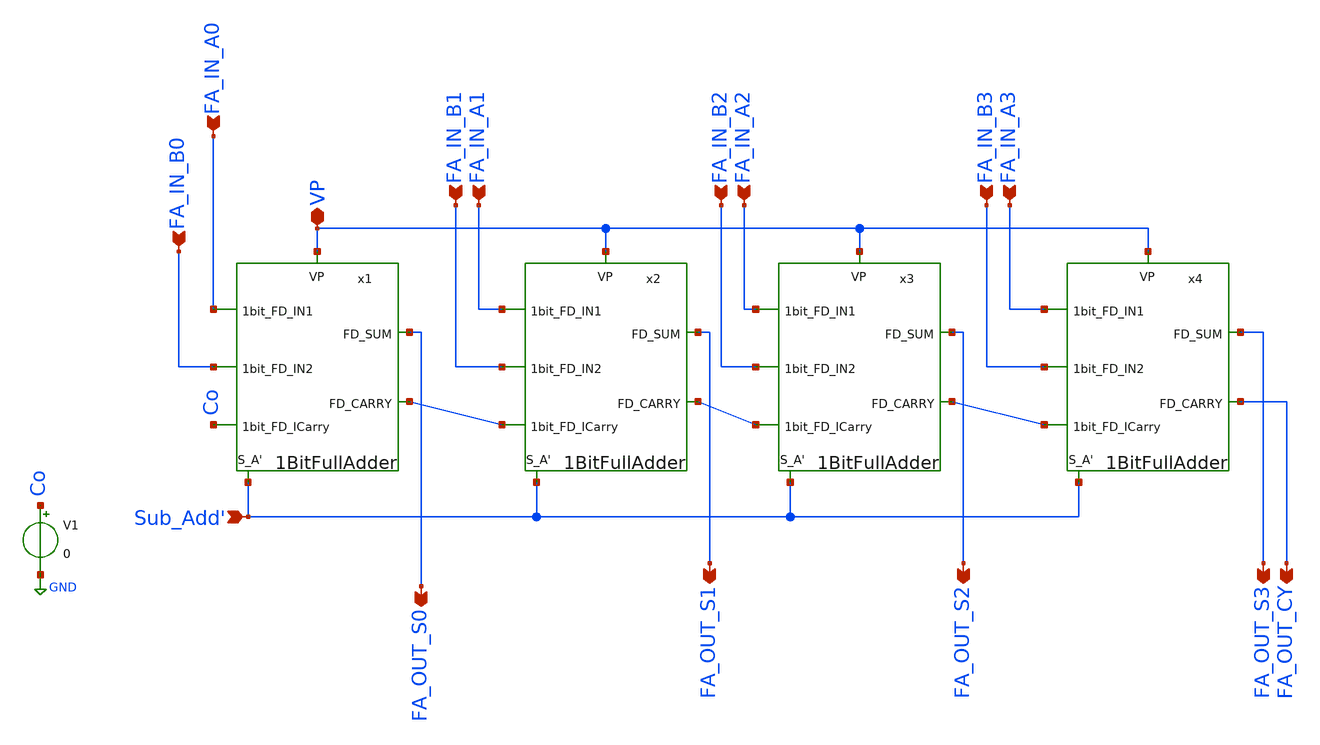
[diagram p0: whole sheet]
** sch_path: AllSymbols&Sch/AdderSubtractor/4bitFullAddSUB.sch
**.subckt 4bitFullAddSUB FA_IN_A0 VP FA_IN_B0 FA_IN_B2 FA_IN_B3 FA_IN_A2 FA_IN_A3 FA_IN_B1 FA_IN_A1 FA_OUT_S0
*+ FA_OUT_S1 FA_OUT_S2 FA_OUT_S3 FA_OUT_CY Sub_Add'
*.ipin FA_IN_A0
*.iopin VP
*.ipin FA_IN_B0
*.ipin FA_IN_B2
*.ipin FA_IN_B3
*.ipin FA_IN_A2
*.ipin FA_IN_A3
*.ipin FA_IN_B1
*.ipin FA_IN_A1
*.opin FA_OUT_S0
*.opin FA_OUT_S1
*.opin FA_OUT_S2
*.opin FA_OUT_S3
*.opin FA_OUT_CY
*.ipin Sub_Add'
V1 Co GND 0
x1 VP FA_IN_A0 FA_IN_B0 Co FA_OUT_S0 net1 Sub_Add' 1BitFullAdder
x2 VP FA_IN_A1 FA_IN_B1 net1 FA_OUT_S1 net2 Sub_Add' 1BitFullAdder
x3 VP FA_IN_A2 FA_IN_B2 net2 FA_OUT_S2 net3 Sub_Add' 1BitFullAdder
x4 VP FA_IN_A3 FA_IN_B3 net3 FA_OUT_S3 FA_OUT_CY Sub_Add' 1BitFullAdder
**.ends

* expanding   symbol:
*+  /home/safal/projects/GitHub_CMOS_4bit_ALU/AllSymbols&Sch/AdderSubtractor/1BitFullAdder.sym # of pins=7
** sym_path: AllSymbols&Sch/AdderSubtractor/1BitFullAdder.sym
** sch_path: AllSymbols&Sch/AdderSubtractor/1BitFullAdder.sch
.subckt 1BitFullAdder VP 1bit_FD_IN1 1bit_FD_IN2 1bit_FD_ICarry FD_SUM FD_CARRY SUB_ADD'
*.ipin 1bit_FD_IN1
*.opin FD_SUM
*.iopin VP
*.ipin 1bit_FD_IN2
*.ipin 1bit_FD_ICarry
*.opin FD_CARRY
*.ipin SUB_ADD'
x5 net1 VP 1bit_FD_ICarry FD_SUM XORTransmissonGate
x6 1bit_FD_IN2 VP 1bit_FD_IN1 net1 XORTransmissonGate
x10 1bit_FD_IN1 VP SUB_ADD' net5 XORTransmissonGate
x1 net4 net3 FD_CARRY VP StaticORGate
x2 net4 net2 1bit_FD_ICarry VP StaticAndGate
x4 SUB_ADD' VP net1 net2 XORTransmissonGate
x7 net3 1bit_FD_IN2 net5 VP StaticAndGate
.ends


* expanding   symbol:
*+  /home/safal/projects/GitHub_CMOS_4bit_ALU/AllSymbols&Sch/Gates/XORTransmissonGate.sym # of pins=4
** sym_path: AllSymbols&Sch/Gates/XORTransmissonGate.sym
** sch_path: AllSymbols&Sch/Gates/XORTransmissonGate.sch
.subckt XORTransmissonGate XOR_IN1 VP XOR_IN2 XOR_OUT
*.ipin XOR_IN2
*.ipin XOR_IN1
*.opin XOR_OUT
*.iopin VP
x1 XOR_IN1 VP XOR_IN2 XOR_OUT GND net1 TransmissionGate
x2 net1 VP net2 XOR_OUT GND XOR_IN1 TransmissionGate
x3 VP net2 XOR_IN2 inverter
x4 VP net1 XOR_IN1 inverter
.ends


* expanding   symbol:
*+  /home/safal/projects/GitHub_CMOS_4bit_ALU/AllSymbols&Sch/Gates/StaticORGate.sym # of pins=4
** sym_path: AllSymbols&Sch/Gates/StaticORGate.sym
** sch_path: AllSymbols&Sch/Gates/StaticORGate.sch
.subckt StaticORGate OR_IN2 OR_IN1 OR_OUT VP
*.ipin OR_IN1
*.opin OR_OUT
*.ipin OR_IN2
*.iopin VP
XM1 net2 OR_IN1 net1 net1 sky130_fd_pr__pfet_01v8 L=0.15 W=8 nf=1 ad='int((1 + 1)/2) * 8 / 1 * 0.29'
+ as='int((1 + 2)/2) * 8 / 1 * 0.29' pd='2*int((1 + 1)/2) * (8 / 1 + 0.29)' ps='2*int((1 + 2)/2) * (8 / 1 + 0.29)'
+ nrd='0.29 / 8 ' nrs='0.29 / 8 ' sa=0 sb=0 sd=0 mult=1 m=1
XM2 net2 OR_IN1 GND GND sky130_fd_pr__nfet_01v8 L=0.15 W=1 nf=1 ad='int((1 + 1)/2) * 1 / 1 * 0.29' as='int((1 + 2)/2) * 1 / 1 * 0.29'
+ pd='2*int((1 + 1)/2) * (1 / 1 + 0.29)' ps='2*int((1 + 2)/2) * (1 / 1 + 0.29)' nrd='0.29 / 1 ' nrs='0.29 / 1 '
+ sa=0 sb=0 sd=0 mult=1 m=1
XM5 net1 OR_IN2 VP VP sky130_fd_pr__pfet_01v8 L=0.15 W=8 nf=1 ad='int((1 + 1)/2) * 8 / 1 * 0.29' as='int((1 + 2)/2) * 8 / 1 * 0.29'
+ pd='2*int((1 + 1)/2) * (8 / 1 + 0.29)' ps='2*int((1 + 2)/2) * (8 / 1 + 0.29)' nrd='0.29 / 8 ' nrs='0.29 / 8 '
+ sa=0 sb=0 sd=0 mult=1 m=1
XM6 net2 OR_IN2 GND GND sky130_fd_pr__nfet_01v8 L=0.15 W=1 nf=1 ad='int((1 + 1)/2) * 1 / 1 * 0.29' as='int((1 + 2)/2) * 1 / 1 * 0.29'
+ pd='2*int((1 + 1)/2) * (1 / 1 + 0.29)' ps='2*int((1 + 2)/2) * (1 / 1 + 0.29)' nrd='0.29 / 1 ' nrs='0.29 / 1 '
+ sa=0 sb=0 sd=0 mult=1 m=1
x1 VP OR_OUT net2 inverter
.ends


* expanding   symbol:
*+  /home/safal/projects/GitHub_CMOS_4bit_ALU/AllSymbols&Sch/Gates/StaticAndGate.sym # of pins=4
** sym_path: AllSymbols&Sch/Gates/StaticAndGate.sym
** sch_path: AllSymbols&Sch/Gates/StaticAndGate.sch
.subckt StaticAndGate ANDOUT AND_IN1 AND_IN2 VP
*.ipin AND_IN1
*.opin ANDOUT
*.ipin AND_IN2
*.iopin VP
XM1 net2 AND_IN2 VP VP sky130_fd_pr__pfet_01v8 L=0.15 W=1 nf=1 ad='int((1 + 1)/2) * 1 / 1 * 0.29' as='int((1 + 2)/2) * 1 / 1 * 0.29'
+ pd='2*int((1 + 1)/2) * (1 / 1 + 0.29)' ps='2*int((1 + 2)/2) * (1 / 1 + 0.29)' nrd='0.29 / 1 ' nrs='0.29 / 1 '
+ sa=0 sb=0 sd=0 mult=1 m=1
XM2 net2 AND_IN1 net1 net1 sky130_fd_pr__nfet_01v8 L=0.15 W=2 nf=1 ad='int((1 + 1)/2) * 2 / 1 * 0.29'
+ as='int((1 + 2)/2) * 2 / 1 * 0.29' pd='2*int((1 + 1)/2) * (2 / 1 + 0.29)' ps='2*int((1 + 2)/2) * (2 / 1 + 0.29)'
+ nrd='0.29 / 2 ' nrs='0.29 / 2 ' sa=0 sb=0 sd=0 mult=1 m=1
XM3 net1 AND_IN2 GND GND sky130_fd_pr__nfet_01v8 L=0.15 W=2 nf=1 ad='int((1 + 1)/2) * 2 / 1 * 0.29' as='int((1 + 2)/2) * 2 / 1 * 0.29'
+ pd='2*int((1 + 1)/2) * (2 / 1 + 0.29)' ps='2*int((1 + 2)/2) * (2 / 1 + 0.29)' nrd='0.29 / 2 ' nrs='0.29 / 2 '
+ sa=0 sb=0 sd=0 mult=1 m=1
XM4 net2 AND_IN1 VP VP sky130_fd_pr__pfet_01v8 L=0.15 W=1 nf=1 ad='int((1 + 1)/2) * 1 / 1 * 0.29' as='int((1 + 2)/2) * 1 / 1 * 0.29'
+ pd='2*int((1 + 1)/2) * (1 / 1 + 0.29)' ps='2*int((1 + 2)/2) * (1 / 1 + 0.29)' nrd='0.29 / 1 ' nrs='0.29 / 1 '
+ sa=0 sb=0 sd=0 mult=1 m=1
x1 VP ANDOUT net2 inverter
.ends


* expanding   symbol:
*+  /home/safal/projects/GitHub_CMOS_4bit_ALU/AllSymbols&Sch/GenericSym/TransmissionGate.sym # of pins=6
** sym_path: AllSymbols&Sch/GenericSym/TransmissionGate.sym
** sch_path: AllSymbols&Sch/GenericSym/TransmissionGate.sch
.subckt TransmissionGate X VP A Y VN X'
*.ipin A
*.opin Y
*.ipin X'
*.ipin X
*.iopin VP
*.iopin VN
XM1 A X Y VP sky130_fd_pr__pfet_01v8 L=0.15 W=1 nf=1 ad='int((1 + 1)/2) * 1 / 1 * 0.29' as='int((1 + 2)/2) * 1 / 1 * 0.29'
+ pd='2*int((1 + 1)/2) * (1 / 1 + 0.29)' ps='2*int((1 + 2)/2) * (1 / 1 + 0.29)' nrd='0.29 / 1 ' nrs='0.29 / 1 '
+ sa=0 sb=0 sd=0 mult=1 m=1
XM2 A X' Y VN sky130_fd_pr__nfet_01v8 L=0.15 W=1 nf=1 ad='int((1 + 1)/2) * 1 / 1 * 0.29' as='int((1 +
+ 2)/2) * 1 / 1 * 0.29' pd='2*int((1 + 1)/2) * (1 / 1 + 0.29)' ps='2*int((1 + 2)/2) * (1 / 1 + 0.29)' nrd='0.29
+ / 1 ' nrs='0.29 / 1 ' sa=0 sb=0 sd=0 mult=1 m=1
**** begin user architecture code

.lib /usr/local/share/pdk/sky130A/libs.tech/ngspice/sky130.lib.spice tt

**** end user architecture code
.ends


* expanding   symbol:  /home/safal/projects/GitHub_CMOS_4bit_ALU/AllSymbols&Sch/GenericSym/inverter.sym # of pins=3
** sym_path: AllSymbols&Sch/GenericSym/inverter.sym
** sch_path: AllSymbols&Sch/GenericSym/inverter.sch
.subckt inverter VP inv_out inv_in
*.ipin inv_in
*.opin inv_out
*.iopin VP
XM1 inv_out inv_in VP VP sky130_fd_pr__pfet_01v8 L=0.15 W=2 nf=1 ad='int((1 + 1)/2) * 2 / 1 * 0.29' as='int((1
+ + 2)/2) * 2 / 1 * 0.29' pd='2*int((1 + 1)/2) * (2 / 1 + 0.29)' ps='2*int((1 + 2)/2) * (2 / 1 + 0.29)' nrd='0.29
+ / 2 ' nrs='0.29 / 2 ' sa=0 sb=0 sd=0 mult=1 m=1
XM2 inv_out inv_in GND GND sky130_fd_pr__nfet_01v8 L=0.15 W=1 nf=1 ad='int((1 + 1)/2) * 1 / 1 * 0.29' as='int((1
+ + 2)/2) * 1 / 1 * 0.29' pd='2*int((1 + 1)/2) * (1 / 1 + 0.29)' ps='2*int((1 + 2)/2) * (1 / 1 + 0.29)' nrd='0.29
+ / 1 ' nrs='0.29 / 1 ' sa=0 sb=0 sd=0 mult=1 m=1
.ends

.GLOBAL GND
.end
